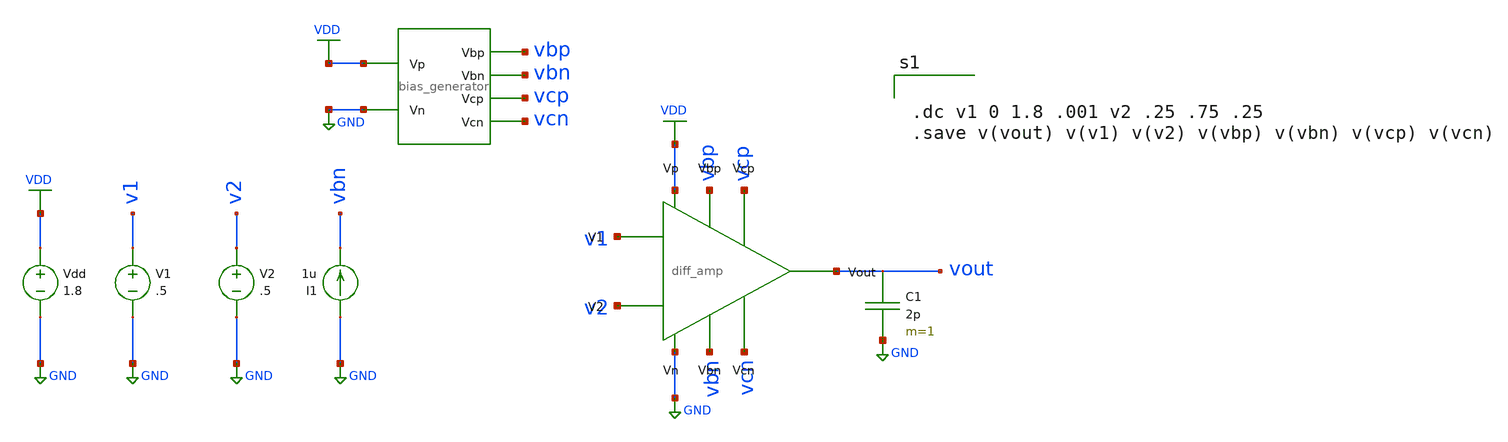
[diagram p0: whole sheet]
** sch_path: mini_proj_3/schematic/diff_testbench.sch
**.subckt diff_testbench
Vdd VDD GND 1.8
V1 v1 GND .5
V2 v2 GND .5
I1 GND vbn 1u
X1 VDD GND vbp vbn vcp vcn bias_generator
X3 VDD GND vbp vbn vcp vcn v1 v2 vout diff_amp
C1 vout GND 2p m=1
**** begin user architecture code

.option wnflag=1
.lib ~/skywater/skywater-pdk/libraries/sky130_fd_pr_ngspice/latest/models/sky130.lib.spice tt



.dc v1 0 1.8 .001 v2 .25 .75 .25
.save v(vout) v(v1) v(v2) v(vbp) v(vbn) v(vcp) v(vcn)

**** end user architecture code
**.ends
.GLOBAL GND
.GLOBAL VDD
.end
